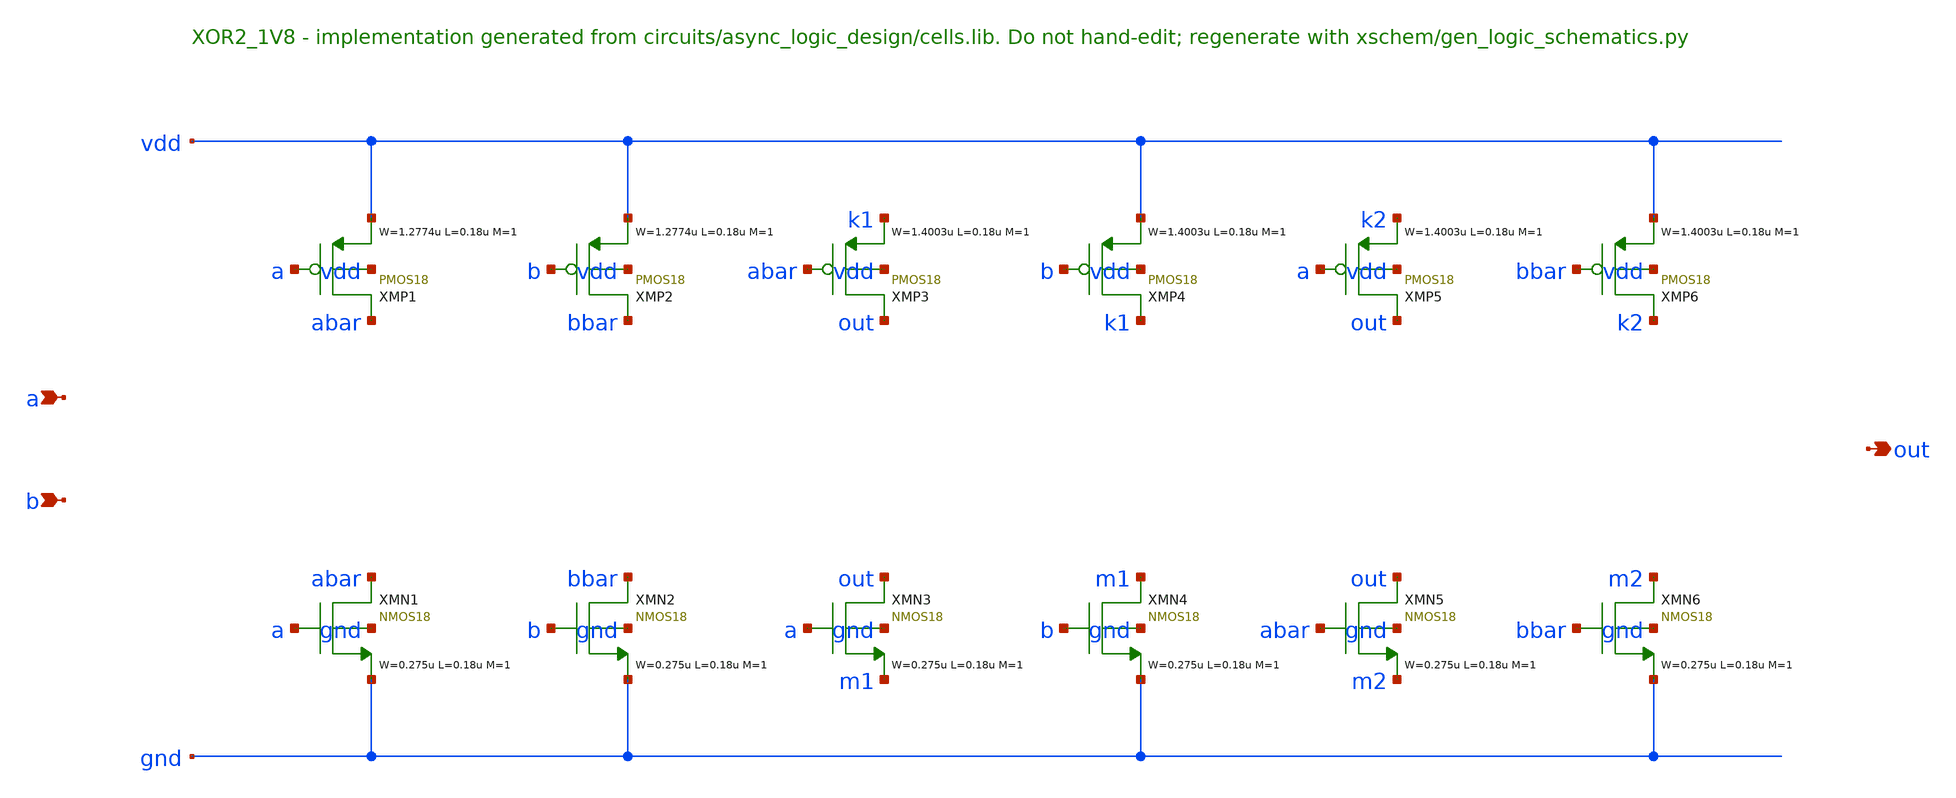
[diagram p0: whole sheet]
** sch_path: xschem/logic/XOR2_1V8.sch
**.subckt XOR2_1V8 a b out
*.ipin a
*.ipin b
*.opin out
XMP1 abar a vdd vdd PMOS18 W=1.2774u L=0.18u M=1 MM_SIGMA=0
XMP2 bbar b vdd vdd PMOS18 W=1.2774u L=0.18u M=1 MM_SIGMA=0
XMP3 out abar k1 vdd PMOS18 W=1.4003u L=0.18u M=1 MM_SIGMA=0
XMP4 k1 b vdd vdd PMOS18 W=1.4003u L=0.18u M=1 MM_SIGMA=0
XMP5 out a k2 vdd PMOS18 W=1.4003u L=0.18u M=1 MM_SIGMA=0
XMP6 k2 bbar vdd vdd PMOS18 W=1.4003u L=0.18u M=1 MM_SIGMA=0
XMN1 abar a gnd gnd NMOS18 W=0.275u L=0.18u M=1 MM_SIGMA=0
XMN2 bbar b gnd gnd NMOS18 W=0.275u L=0.18u M=1 MM_SIGMA=0
XMN3 out a m1 gnd NMOS18 W=0.275u L=0.18u M=1 MM_SIGMA=0
XMN4 m1 b gnd gnd NMOS18 W=0.275u L=0.18u M=1 MM_SIGMA=0
XMN5 out abar m2 gnd NMOS18 W=0.275u L=0.18u M=1 MM_SIGMA=0
XMN6 m2 bbar gnd gnd NMOS18 W=0.275u L=0.18u M=1 MM_SIGMA=0
**.ends
.end
